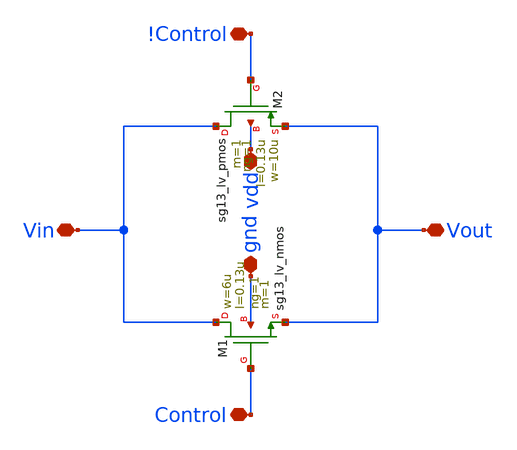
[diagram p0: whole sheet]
** sch_path: dependencies/SAH/SAH-main/schematic/xschem/T_gate.sch
**.subckt T_gate Vout Vin !Control Control gnd vdd
*.iopin Vout
*.iopin Vin
*.iopin !Control
*.iopin Control
*.iopin gnd
*.iopin vdd
XM1 Vin Control Vout gnd sg13_lv_nmos w=6u l=0.13u ng=1 m=1 mm_ok=1
XM2 Vin !Control Vout vdd sg13_lv_pmos w=10u l=0.13u ng=1 m=1 mm_ok=1
**.ends
.end
